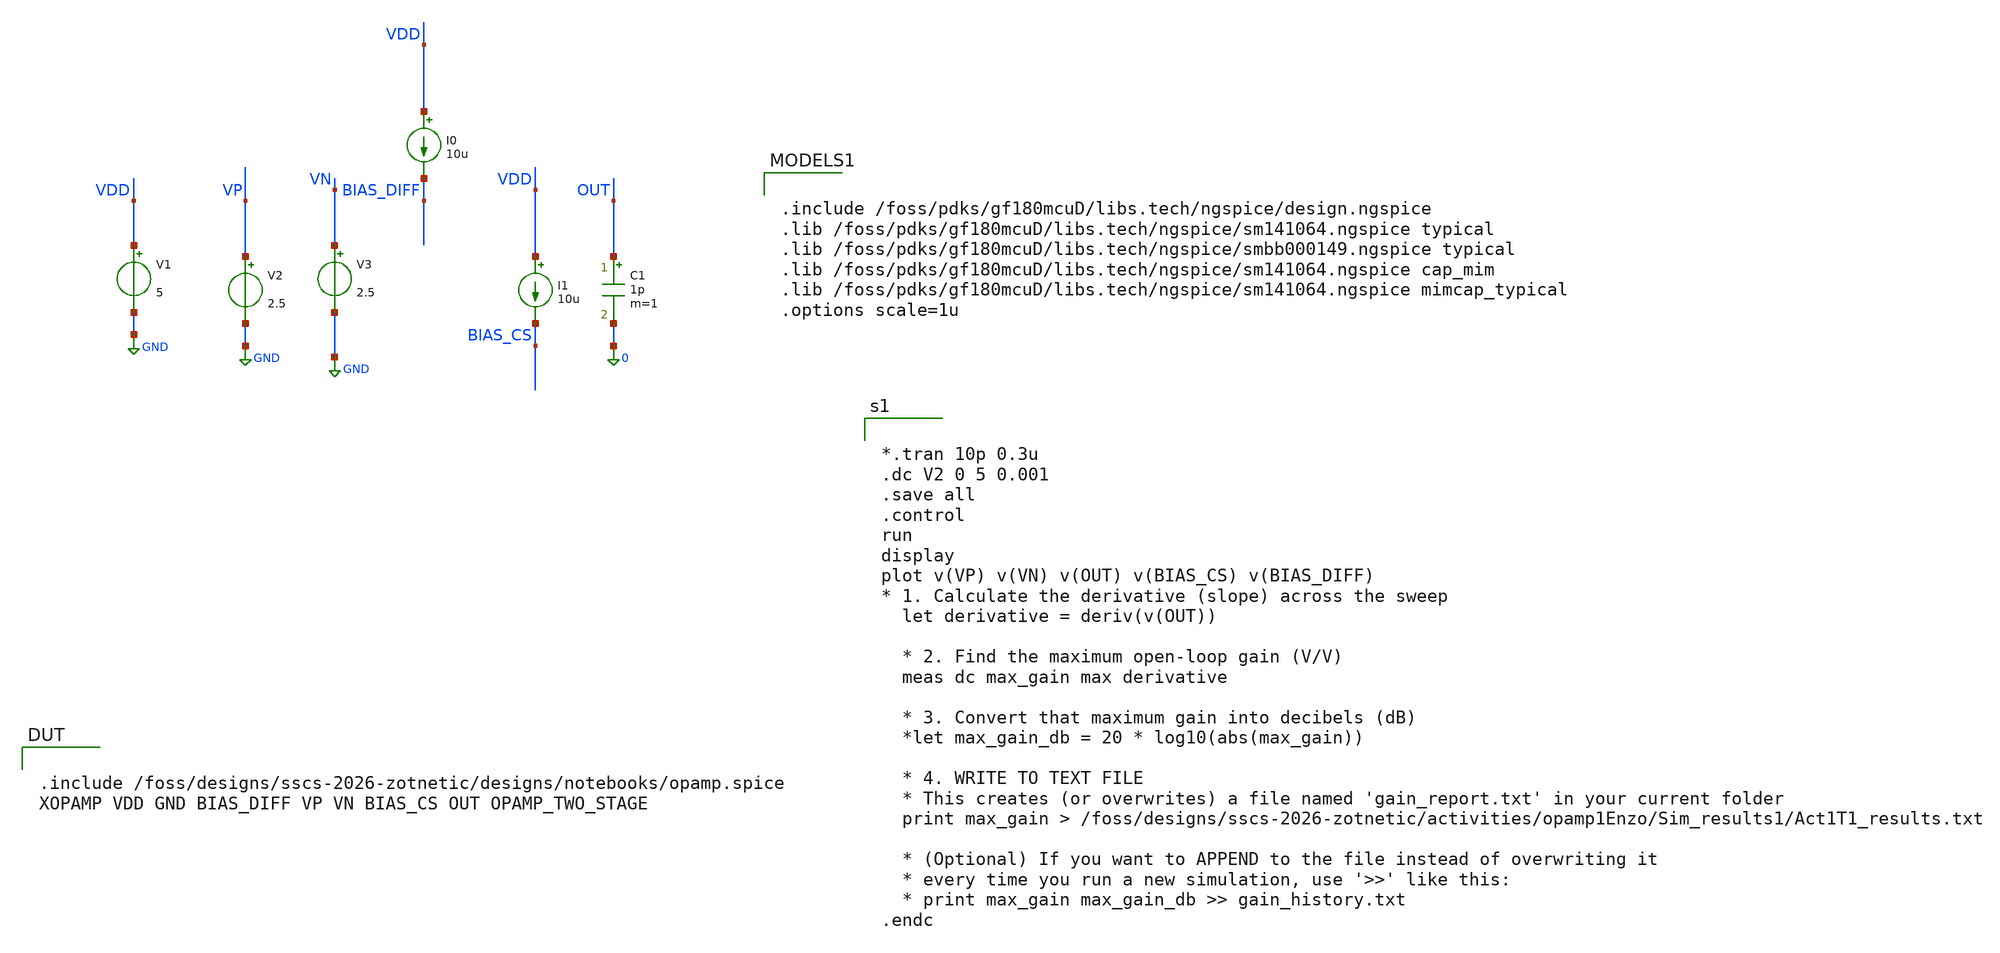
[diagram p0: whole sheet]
** sch_path: activities/opamp1Enzo/Act1T1.sch
**.subckt Act1T1
V1 VDD GND 5
V2 VP GND 2.5
V3 VN GND 2.5
C1 OUT 0 1p m=1
I0 VDD BIAS_DIFF 10u
I1 VDD BIAS_CS 10u
**** begin user architecture code


*.tran 10p 0.3u
.dc V2 0 5 0.001
.save all
.control
run
display
plot v(VP) v(VN) v(OUT) v(BIAS_CS) v(BIAS_DIFF)
* 1. Calculate the derivative (slope) across the sweep
  let derivative = deriv(v(OUT))

  * 2. Find the maximum open-loop gain (V/V)
  meas dc max_gain max derivative

  * 3. Convert that maximum gain into decibels (dB)
  *let max_gain_db = 20 * log10(abs(max_gain))

  * 4. WRITE TO TEXT FILE
  * This creates (or overwrites) a file named 'gain_report.txt' in your current folder
  print max_gain >
+ /foss/designs/sscs-2026-zotnetic/activities/opamp1Enzo/Sim_results1/Act1T1_results.txt

  * (Optional) If you want to APPEND to the file instead of overwriting it
  * every time you run a new simulation, use '>>' like this:
  * print max_gain max_gain_db >> gain_history.txt
.endc




.include /foss/pdks/gf180mcuD/libs.tech/ngspice/design.ngspice
.lib /foss/pdks/gf180mcuD/libs.tech/ngspice/sm141064.ngspice typical
.lib /foss/pdks/gf180mcuD/libs.tech/ngspice/smbb000149.ngspice typical
.lib /foss/pdks/gf180mcuD/libs.tech/ngspice/sm141064.ngspice cap_mim
.lib /foss/pdks/gf180mcuD/libs.tech/ngspice/sm141064.ngspice mimcap_typical
.options scale=1u



.include /foss/designs/sscs-2026-zotnetic/designs/notebooks/opamp.spice
XOPAMP VDD GND BIAS_DIFF VP VN BIAS_CS OUT OPAMP_TWO_STAGE
**** end user architecture code
**.ends
.GLOBAL GND
.end
